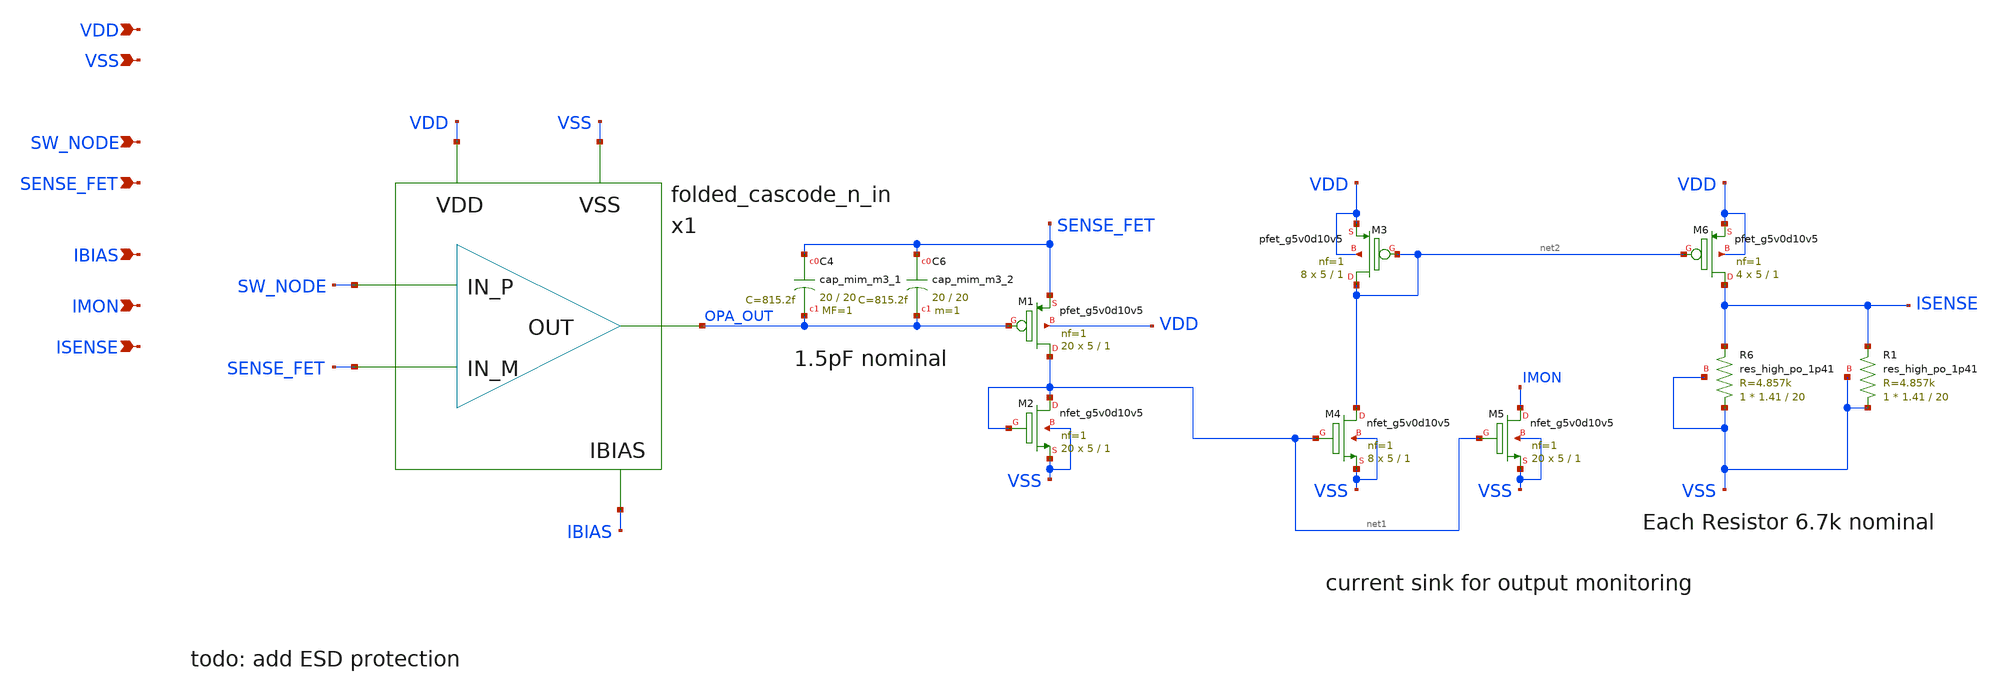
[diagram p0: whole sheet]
** sch_path: design/current-sense/current_sense.sch
**.subckt current_sense SW_NODE SENSE_FET VDD VSS IBIAS IMON ISENSE
*.ipin SW_NODE
*.ipin SENSE_FET
*.ipin VDD
*.ipin VSS
*.ipin IBIAS
*.ipin IMON
*.ipin ISENSE
x1 SW_NODE SENSE_FET OPA_OUT VDD VSS IBIAS folded_cascode_n_in
XM1 net1 OPA_OUT SENSE_FET VDD sky130_fd_pr__pfet_g5v0d10v5 L=1 W=5 nf=1 ad='int((nf+1)/2) * W/nf * 0.29'
+ as='int((nf+2)/2) * W/nf * 0.29' pd='2*int((nf+1)/2) * (W/nf + 0.29)' ps='2*int((nf+2)/2) * (W/nf + 0.29)'
+ nrd='0.29 / W' nrs='0.29 / W' sa=0 sb=0 sd=0 mult=20 m=20
XM2 net1 net1 VSS VSS sky130_fd_pr__nfet_g5v0d10v5 L=1 W=5 nf=1 ad='int((nf+1)/2) * W/nf * 0.29' as='int((nf+2)/2) * W/nf * 0.29'
+ pd='2*int((nf+1)/2) * (W/nf + 0.29)' ps='2*int((nf+2)/2) * (W/nf + 0.29)' nrd='0.29 / W' nrs='0.29 / W'
+ sa=0 sb=0 sd=0 mult=20 m=20
XM4 net2 net1 VSS VSS sky130_fd_pr__nfet_g5v0d10v5 L=1 W=5 nf=1 ad='int((nf+1)/2) * W/nf * 0.29' as='int((nf+2)/2) * W/nf * 0.29'
+ pd='2*int((nf+1)/2) * (W/nf + 0.29)' ps='2*int((nf+2)/2) * (W/nf + 0.29)' nrd='0.29 / W' nrs='0.29 / W'
+ sa=0 sb=0 sd=0 mult=8 m=8
XM3 net2 net2 VDD VDD sky130_fd_pr__pfet_g5v0d10v5 L=1 W=5 nf=1 ad='int((nf+1)/2) * W/nf * 0.29' as='int((nf+2)/2) * W/nf * 0.29'
+ pd='2*int((nf+1)/2) * (W/nf + 0.29)' ps='2*int((nf+2)/2) * (W/nf + 0.29)' nrd='0.29 / W' nrs='0.29 / W'
+ sa=0 sb=0 sd=0 mult=8 m=8
XM5 IMON net1 VSS VSS sky130_fd_pr__nfet_g5v0d10v5 L=1 W=5 nf=1 ad='int((nf+1)/2) * W/nf * 0.29' as='int((nf+2)/2) * W/nf * 0.29'
+ pd='2*int((nf+1)/2) * (W/nf + 0.29)' ps='2*int((nf+2)/2) * (W/nf + 0.29)' nrd='0.29 / W' nrs='0.29 / W'
+ sa=0 sb=0 sd=0 mult=20 m=20
XM6 ISENSE net2 VDD VDD sky130_fd_pr__pfet_g5v0d10v5 L=1 W=5 nf=1 ad='int((nf+1)/2) * W/nf * 0.29' as='int((nf+2)/2) * W/nf * 0.29'
+ pd='2*int((nf+1)/2) * (W/nf + 0.29)' ps='2*int((nf+2)/2) * (W/nf + 0.29)' nrd='0.29 / W' nrs='0.29 / W'
+ sa=0 sb=0 sd=0 mult=4 m=4
XR6 VSS ISENSE VSS sky130_fd_pr__res_high_po_1p41 L=20 mult=1 m=1
XR1 VSS ISENSE VSS sky130_fd_pr__res_high_po_1p41 L=20 mult=1 m=1
XC4 SENSE_FET OPA_OUT sky130_fd_pr__cap_mim_m3_1 W=20 L=20 MF=1 m=1
XC6 SENSE_FET OPA_OUT sky130_fd_pr__cap_mim_m3_2 W=20 L=20 MF=1 m=1
**.ends

* expanding   symbol:  design/folded-cascode-n-in/folded_cascode_n_in.sym # of pins=6
** sym_path: design/folded-cascode-n-in/folded_cascode_n_in.sym
** sch_path: design/folded-cascode-n-in/folded_cascode_n_in.sch
.subckt folded_cascode_n_in IN_P IN_M OUT VDD VSS VBN
*.ipin IN_P
*.ipin IN_M
*.ipin OUT
*.ipin VDD
*.ipin VSS
*.ipin VBN
XM1 net1 VBN VSS VSS sky130_fd_pr__nfet_g5v0d10v5 L=1 W=5 nf=1 ad='int((nf+1)/2) * W/nf * 0.29' as='int((nf+2)/2) * W/nf * 0.29'
+ pd='2*int((nf+1)/2) * (W/nf + 0.29)' ps='2*int((nf+2)/2) * (W/nf + 0.29)' nrd='0.29 / W' nrs='0.29 / W'
+ sa=0 sb=0 sd=0 mult=12 m=12
XM3 VS1_P IN_M net1 VSS sky130_fd_pr__nfet_g5v0d10v5 L=1 W=5 nf=1 ad='int((nf+1)/2) * W/nf * 0.29' as='int((nf+2)/2) * W/nf * 0.29'
+ pd='2*int((nf+1)/2) * (W/nf + 0.29)' ps='2*int((nf+2)/2) * (W/nf + 0.29)' nrd='0.29 / W' nrs='0.29 / W'
+ sa=0 sb=0 sd=0 mult=24 m=24
XM4 VS1_M IN_P net1 VSS sky130_fd_pr__nfet_g5v0d10v5 L=1 W=5 nf=1 ad='int((nf+1)/2) * W/nf * 0.29' as='int((nf+2)/2) * W/nf * 0.29'
+ pd='2*int((nf+1)/2) * (W/nf + 0.29)' ps='2*int((nf+2)/2) * (W/nf + 0.29)' nrd='0.29 / W' nrs='0.29 / W'
+ sa=0 sb=0 sd=0 mult=24 m=24
XM9 net2 VCN net4 VSS sky130_fd_pr__nfet_g5v0d10v5 L=1 W=5 nf=1 ad='int((nf+1)/2) * W/nf * 0.29' as='int((nf+2)/2) * W/nf * 0.29'
+ pd='2*int((nf+1)/2) * (W/nf + 0.29)' ps='2*int((nf+2)/2) * (W/nf + 0.29)' nrd='0.29 / W' nrs='0.29 / W'
+ sa=0 sb=0 sd=0 mult=4 m=4
XM10 net3 net2 VSS VSS sky130_fd_pr__nfet_g5v0d10v5 L=1 W=5 nf=1 ad='int((nf+1)/2) * W/nf * 0.29' as='int((nf+2)/2) * W/nf * 0.29'
+ pd='2*int((nf+1)/2) * (W/nf + 0.29)' ps='2*int((nf+2)/2) * (W/nf + 0.29)' nrd='0.29 / W' nrs='0.29 / W'
+ sa=0 sb=0 sd=0 mult=4 m=4
XM11 net4 net2 VSS VSS sky130_fd_pr__nfet_g5v0d10v5 L=1 W=5 nf=1 ad='int((nf+1)/2) * W/nf * 0.29' as='int((nf+2)/2) * W/nf * 0.29'
+ pd='2*int((nf+1)/2) * (W/nf + 0.29)' ps='2*int((nf+2)/2) * (W/nf + 0.29)' nrd='0.29 / W' nrs='0.29 / W'
+ sa=0 sb=0 sd=0 mult=4 m=4
XM12 OUT VCN net3 VSS sky130_fd_pr__nfet_g5v0d10v5 L=1 W=5 nf=1 ad='int((nf+1)/2) * W/nf * 0.29' as='int((nf+2)/2) * W/nf * 0.29'
+ pd='2*int((nf+1)/2) * (W/nf + 0.29)' ps='2*int((nf+2)/2) * (W/nf + 0.29)' nrd='0.29 / W' nrs='0.29 / W'
+ sa=0 sb=0 sd=0 mult=4 m=4
XM5 VS1_P VBP_INT VDD VDD sky130_fd_pr__pfet_g5v0d10v5 L=1 W=5 nf=1 ad='int((nf+1)/2) * W/nf * 0.29'
+ as='int((nf+2)/2) * W/nf * 0.29' pd='2*int((nf+1)/2) * (W/nf + 0.29)' ps='2*int((nf+2)/2) * (W/nf + 0.29)'
+ nrd='0.29 / W' nrs='0.29 / W' sa=0 sb=0 sd=0 mult=10 m=10
XM13 VS1_M VBP_INT VDD VDD sky130_fd_pr__pfet_g5v0d10v5 L=1 W=5 nf=1 ad='int((nf+1)/2) * W/nf * 0.29'
+ as='int((nf+2)/2) * W/nf * 0.29' pd='2*int((nf+1)/2) * (W/nf + 0.29)' ps='2*int((nf+2)/2) * (W/nf + 0.29)'
+ nrd='0.29 / W' nrs='0.29 / W' sa=0 sb=0 sd=0 mult=10 m=10
XM17 VBP_INT VBN VSS VSS sky130_fd_pr__nfet_g5v0d10v5 L=1 W=5 nf=1 ad='int((nf+1)/2) * W/nf * 0.29' as='int((nf+2)/2) * W/nf * 0.29'
+ pd='2*int((nf+1)/2) * (W/nf + 0.29)' ps='2*int((nf+2)/2) * (W/nf + 0.29)' nrd='0.29 / W' nrs='0.29 / W'
+ sa=0 sb=0 sd=0 mult=1 m=1
XM18 VBP_INT VBP_INT VDD VDD sky130_fd_pr__pfet_g5v0d10v5 L=1 W=5 nf=1 ad='int((nf+1)/2) * W/nf * 0.29'
+ as='int((nf+2)/2) * W/nf * 0.29' pd='2*int((nf+1)/2) * (W/nf + 0.29)' ps='2*int((nf+2)/2) * (W/nf + 0.29)'
+ nrd='0.29 / W' nrs='0.29 / W' sa=0 sb=0 sd=0 mult=1 m=1
XM14 net2 VCP VS1_M VDD sky130_fd_pr__pfet_g5v0d10v5 L=1 W=5 nf=1 ad='int((nf+1)/2) * W/nf * 0.29' as='int((nf+2)/2) * W/nf * 0.29'
+ pd='2*int((nf+1)/2) * (W/nf + 0.29)' ps='2*int((nf+2)/2) * (W/nf + 0.29)' nrd='0.29 / W' nrs='0.29 / W'
+ sa=0 sb=0 sd=0 mult=4 m=4
XM19 OUT VCP VS1_P VDD sky130_fd_pr__pfet_g5v0d10v5 L=1 W=5 nf=1 ad='int((nf+1)/2) * W/nf * 0.29' as='int((nf+2)/2) * W/nf * 0.29'
+ pd='2*int((nf+1)/2) * (W/nf + 0.29)' ps='2*int((nf+2)/2) * (W/nf + 0.29)' nrd='0.29 / W' nrs='0.29 / W'
+ sa=0 sb=0 sd=0 mult=4 m=4
XM2 VBP_INT VBP_INT VS1_P VSS sky130_fd_pr__nfet_g5v0d10v5 L=1 W=5 nf=1 ad='int((nf+1)/2) * W/nf * 0.29'
+ as='int((nf+2)/2) * W/nf * 0.29' pd='2*int((nf+1)/2) * (W/nf + 0.29)' ps='2*int((nf+2)/2) * (W/nf + 0.29)'
+ nrd='0.29 / W' nrs='0.29 / W' sa=0 sb=0 sd=0 mult=1 m=1
XM6 VBP_INT VBP_INT VS1_M VSS sky130_fd_pr__nfet_g5v0d10v5 L=1 W=5 nf=1 ad='int((nf+1)/2) * W/nf * 0.29'
+ as='int((nf+2)/2) * W/nf * 0.29' pd='2*int((nf+1)/2) * (W/nf + 0.29)' ps='2*int((nf+2)/2) * (W/nf + 0.29)'
+ nrd='0.29 / W' nrs='0.29 / W' sa=0 sb=0 sd=0 mult=1 m=1
x1 VBN VCN net5 VCP VDD VSS cascode_bias
.ends


* expanding   symbol:  design/bias-circuit/cascode_bias.sym # of pins=6
** sym_path: design/bias-circuit/cascode_bias.sym
** sch_path: design/bias-circuit/cascode_bias.sch
.subckt cascode_bias VBN VCN VBP VCP VDD VSS
*.ipin VCN
*.ipin VBP
*.ipin VCP
*.ipin VDD
*.ipin VSS
*.ipin VBN
XM1 VBP VBP VDD VDD sky130_fd_pr__pfet_g5v0d10v5 L=1 W=5 nf=1 ad='int((nf+1)/2) * W/nf * 0.29' as='int((nf+2)/2) * W/nf * 0.29'
+ pd='2*int((nf+1)/2) * (W/nf + 0.29)' ps='2*int((nf+2)/2) * (W/nf + 0.29)' nrd='0.29 / W' nrs='0.29 / W'
+ sa=0 sb=0 sd=0 mult=1 m=1
XM2 net1 VBP net8 VDD sky130_fd_pr__pfet_g5v0d10v5 L=1 W=5 nf=1 ad='int((nf+1)/2) * W/nf * 0.29' as='int((nf+2)/2) * W/nf * 0.29'
+ pd='2*int((nf+1)/2) * (W/nf + 0.29)' ps='2*int((nf+2)/2) * (W/nf + 0.29)' nrd='0.29 / W' nrs='0.29 / W'
+ sa=0 sb=0 sd=0 mult=1 m=1
XM3 VCN VBP VDD VDD sky130_fd_pr__pfet_g5v0d10v5 L=1 W=5 nf=1 ad='int((nf+1)/2) * W/nf * 0.29' as='int((nf+2)/2) * W/nf * 0.29'
+ pd='2*int((nf+1)/2) * (W/nf + 0.29)' ps='2*int((nf+2)/2) * (W/nf + 0.29)' nrd='0.29 / W' nrs='0.29 / W'
+ sa=0 sb=0 sd=0 mult=1 m=1
XM4 net1 net1 net2 VSS sky130_fd_pr__nfet_g5v0d10v5 L=1 W=5 nf=1 ad='int((nf+1)/2) * W/nf * 0.29' as='int((nf+2)/2) * W/nf * 0.29'
+ pd='2*int((nf+1)/2) * (W/nf + 0.29)' ps='2*int((nf+2)/2) * (W/nf + 0.29)' nrd='0.29 / W' nrs='0.29 / W'
+ sa=0 sb=0 sd=0 mult=2 m=2
XM5 net2 net1 VSS VSS sky130_fd_pr__nfet_g5v0d10v5 L=1 W=5 nf=1 ad='int((nf+1)/2) * W/nf * 0.29' as='int((nf+2)/2) * W/nf * 0.29'
+ pd='2*int((nf+1)/2) * (W/nf + 0.29)' ps='2*int((nf+2)/2) * (W/nf + 0.29)' nrd='0.29 / W' nrs='0.29 / W'
+ sa=0 sb=0 sd=0 mult=1 m=1
XM21 VCN VCN net2 VSS sky130_fd_pr__nfet_g5v0d10v5 L=1 W=5 nf=1 ad='int((nf+1)/2) * W/nf * 0.29' as='int((nf+2)/2) * W/nf * 0.29'
+ pd='2*int((nf+1)/2) * (W/nf + 0.29)' ps='2*int((nf+2)/2) * (W/nf + 0.29)' nrd='0.29 / W' nrs='0.29 / W'
+ sa=0 sb=0 sd=0 mult=1 m=1
XM6 net3 VBN net6 VSS sky130_fd_pr__nfet_g5v0d10v5 L=1 W=5 nf=1 ad='int((nf+1)/2) * W/nf * 0.29' as='int((nf+2)/2) * W/nf * 0.29'
+ pd='2*int((nf+1)/2) * (W/nf + 0.29)' ps='2*int((nf+2)/2) * (W/nf + 0.29)' nrd='0.29 / W' nrs='0.29 / W'
+ sa=0 sb=0 sd=0 mult=1 m=1
XM9 VCP VBN VSS VSS sky130_fd_pr__nfet_g5v0d10v5 L=1 W=5 nf=1 ad='int((nf+1)/2) * W/nf * 0.29' as='int((nf+2)/2) * W/nf * 0.29'
+ pd='2*int((nf+1)/2) * (W/nf + 0.29)' ps='2*int((nf+2)/2) * (W/nf + 0.29)' nrd='0.29 / W' nrs='0.29 / W'
+ sa=0 sb=0 sd=0 mult=1 m=1
XM10 net3 net3 net4 VDD sky130_fd_pr__pfet_g5v0d10v5 L=1 W=5 nf=1 ad='int((nf+1)/2) * W/nf * 0.29' as='int((nf+2)/2) * W/nf * 0.29'
+ pd='2*int((nf+1)/2) * (W/nf + 0.29)' ps='2*int((nf+2)/2) * (W/nf + 0.29)' nrd='0.29 / W' nrs='0.29 / W'
+ sa=0 sb=0 sd=0 mult=2 m=2
XM11 VCP VCP net4 VDD sky130_fd_pr__pfet_g5v0d10v5 L=1 W=5 nf=1 ad='int((nf+1)/2) * W/nf * 0.29' as='int((nf+2)/2) * W/nf * 0.29'
+ pd='2*int((nf+1)/2) * (W/nf + 0.29)' ps='2*int((nf+2)/2) * (W/nf + 0.29)' nrd='0.29 / W' nrs='0.29 / W'
+ sa=0 sb=0 sd=0 mult=1 m=1
XM28 net4 net3 VDD VDD sky130_fd_pr__pfet_g5v0d10v5 L=1 W=5 nf=1 ad='int((nf+1)/2) * W/nf * 0.29' as='int((nf+2)/2) * W/nf * 0.29'
+ pd='2*int((nf+1)/2) * (W/nf + 0.29)' ps='2*int((nf+2)/2) * (W/nf + 0.29)' nrd='0.29 / W' nrs='0.29 / W'
+ sa=0 sb=0 sd=0 mult=1 m=1
XM12 VBP VBN VSS VSS sky130_fd_pr__nfet_g5v0d10v5 L=1 W=5 nf=1 ad='int((nf+1)/2) * W/nf * 0.29' as='int((nf+2)/2) * W/nf * 0.29'
+ pd='2*int((nf+1)/2) * (W/nf + 0.29)' ps='2*int((nf+2)/2) * (W/nf + 0.29)' nrd='0.29 / W' nrs='0.29 / W'
+ sa=0 sb=0 sd=0 mult=1 m=1
XM32 net8 VBP net5 VDD sky130_fd_pr__pfet_g5v0d10v5 L=1 W=5 nf=1 ad='int((nf+1)/2) * W/nf * 0.29' as='int((nf+2)/2) * W/nf * 0.29'
+ pd='2*int((nf+1)/2) * (W/nf + 0.29)' ps='2*int((nf+2)/2) * (W/nf + 0.29)' nrd='0.29 / W' nrs='0.29 / W'
+ sa=0 sb=0 sd=0 mult=1 m=1
XM33 net5 VBP VDD VDD sky130_fd_pr__pfet_g5v0d10v5 L=1 W=5 nf=1 ad='int((nf+1)/2) * W/nf * 0.29' as='int((nf+2)/2) * W/nf * 0.29'
+ pd='2*int((nf+1)/2) * (W/nf + 0.29)' ps='2*int((nf+2)/2) * (W/nf + 0.29)' nrd='0.29 / W' nrs='0.29 / W'
+ sa=0 sb=0 sd=0 mult=1 m=1
XM34 net6 VBN net7 VSS sky130_fd_pr__nfet_g5v0d10v5 L=1 W=5 nf=1 ad='int((nf+1)/2) * W/nf * 0.29' as='int((nf+2)/2) * W/nf * 0.29'
+ pd='2*int((nf+1)/2) * (W/nf + 0.29)' ps='2*int((nf+2)/2) * (W/nf + 0.29)' nrd='0.29 / W' nrs='0.29 / W'
+ sa=0 sb=0 sd=0 mult=1 m=1
XM35 net7 VBN VSS VSS sky130_fd_pr__nfet_g5v0d10v5 L=1 W=5 nf=1 ad='int((nf+1)/2) * W/nf * 0.29' as='int((nf+2)/2) * W/nf * 0.29'
+ pd='2*int((nf+1)/2) * (W/nf + 0.29)' ps='2*int((nf+2)/2) * (W/nf + 0.29)' nrd='0.29 / W' nrs='0.29 / W'
+ sa=0 sb=0 sd=0 mult=1 m=1
XM13 VBN VBN VSS VSS sky130_fd_pr__nfet_g5v0d10v5 L=1 W=5 nf=1 ad='int((nf+1)/2) * W/nf * 0.29' as='int((nf+2)/2) * W/nf * 0.29'
+ pd='2*int((nf+1)/2) * (W/nf + 0.29)' ps='2*int((nf+2)/2) * (W/nf + 0.29)' nrd='0.29 / W' nrs='0.29 / W'
+ sa=0 sb=0 sd=0 mult=1 m=1
.ends

.end
